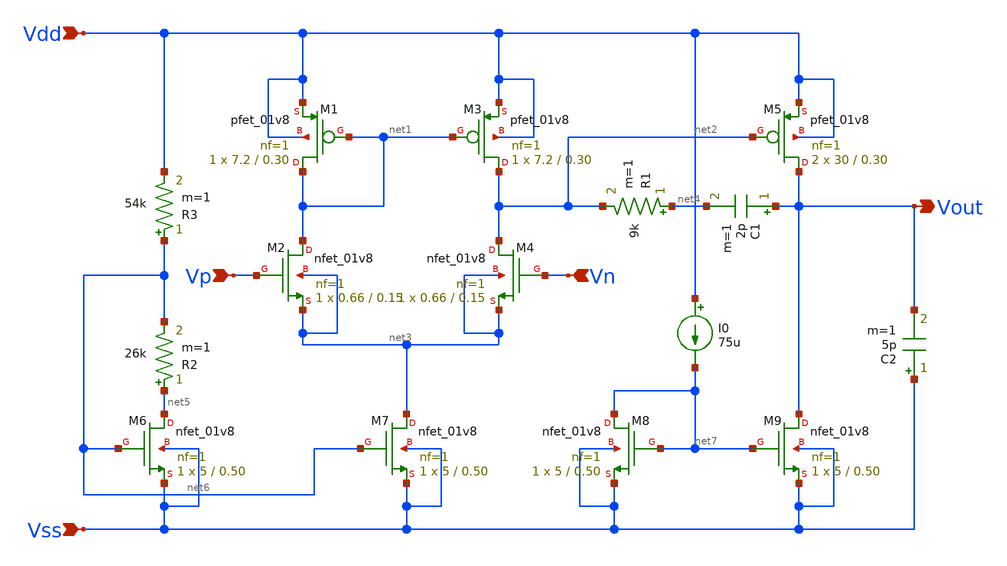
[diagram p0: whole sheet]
** sch_path: Bandgap/No_Ideal/two_stage.sch
**.subckt two_stage Vdd Vout Vss Vp Vn
*.ipin Vdd
*.opin Vout
*.ipin Vss
*.ipin Vp
*.ipin Vn
XM1 net1 net1 Vdd Vdd sky130_fd_pr__pfet_01v8 L=0.30 W=7.2 nf=1 ad='int((1 + 1)/2) * 7.2 / 1 * 0.29'
+ as='int((1 + 2)/2) * 7.2 / 1 * 0.29' pd='2*int((1 + 1)/2) * (7.2 / 1 + 0.29)' ps='2*int((1 + 2)/2) * (7.2 / 1 + 0.29)'
+ nrd='0.29 / 7.2 ' nrs='0.29 / 7.2 ' sa=0 sb=0 sd=0 mult=1 m=1
XM2 net1 Vp net3 net3 sky130_fd_pr__nfet_01v8 L=0.15 W=0.66 nf=1 ad='int((1 + 1)/2) * 0.66 / 1 * 0.29'
+ as='int((1 + 2)/2) * 0.66 / 1 * 0.29' pd='2*int((1 + 1)/2) * (0.66 / 1 + 0.29)' ps='2*int((1 + 2)/2) * (0.66 / 1 + 0.29)'
+ nrd='0.29 / 0.66 ' nrs='0.29 / 0.66 ' sa=0 sb=0 sd=0 mult=1 m=1
XM3 net2 net1 Vdd Vdd sky130_fd_pr__pfet_01v8 L=0.30 W=7.2 nf=1 ad='int((1 + 1)/2) * 7.2 / 1 * 0.29'
+ as='int((1 + 2)/2) * 7.2 / 1 * 0.29' pd='2*int((1 + 1)/2) * (7.2 / 1 + 0.29)' ps='2*int((1 + 2)/2) * (7.2 / 1 + 0.29)'
+ nrd='0.29 / 7.2 ' nrs='0.29 / 7.2 ' sa=0 sb=0 sd=0 mult=1 m=1
XM4 net2 Vn net3 net3 sky130_fd_pr__nfet_01v8 L=0.15 W=0.66 nf=1 ad='int((1 + 1)/2) * 0.66 / 1 * 0.29'
+ as='int((1 + 2)/2) * 0.66 / 1 * 0.29' pd='2*int((1 + 1)/2) * (0.66 / 1 + 0.29)' ps='2*int((1 + 2)/2) * (0.66 / 1 + 0.29)'
+ nrd='0.29 / 0.66 ' nrs='0.29 / 0.66 ' sa=0 sb=0 sd=0 mult=1 m=1
XM5 Vout net2 Vdd Vdd sky130_fd_pr__pfet_01v8 L=0.30 W=30 nf=1 ad='int((1 + 1)/2) * 30 / 1 * 0.29' as='int((1 + 2)/2) * 30 / 1 * 0.29'
+ pd='2*int((1 + 1)/2) * (30 / 1 + 0.29)' ps='2*int((1 + 2)/2) * (30 / 1 + 0.29)' nrd='0.29 / 30 ' nrs='0.29 / 30 '
+ sa=0 sb=0 sd=0 mult=2 m=2
C1 Vout net4 2p m=1
R1 net4 net2 9k m=1
C2 Vss Vout 5p m=1
R2 net5 net6 26k m=1
R3 net6 Vdd 54k m=1
XM6 net5 net6 Vss Vss sky130_fd_pr__nfet_01v8 L=0.50 W=5 nf=1 ad='int((1 + 1)/2) * 5 / 1 * 0.29' as='int((1 + 2)/2) * 5 / 1 * 0.29'
+ pd='2*int((1 + 1)/2) * (5 / 1 + 0.29)' ps='2*int((1 + 2)/2) * (5 / 1 + 0.29)' nrd='0.29 / 5 ' nrs='0.29 / 5 '
+ sa=0 sb=0 sd=0 mult=1 m=1
XM7 net3 net6 Vss Vss sky130_fd_pr__nfet_01v8 L=0.50 W=5 nf=1 ad='int((1 + 1)/2) * 5 / 1 * 0.29' as='int((1 + 2)/2) * 5 / 1 * 0.29'
+ pd='2*int((1 + 1)/2) * (5 / 1 + 0.29)' ps='2*int((1 + 2)/2) * (5 / 1 + 0.29)' nrd='0.29 / 5 ' nrs='0.29 / 5 '
+ sa=0 sb=0 sd=0 mult=1 m=1
XM8 net7 net7 Vss Vss sky130_fd_pr__nfet_01v8 L=0.50 W=5 nf=1 ad='int((1 + 1)/2) * 5 / 1 * 0.29' as='int((1 + 2)/2) * 5 / 1 * 0.29'
+ pd='2*int((1 + 1)/2) * (5 / 1 + 0.29)' ps='2*int((1 + 2)/2) * (5 / 1 + 0.29)' nrd='0.29 / 5 ' nrs='0.29 / 5 '
+ sa=0 sb=0 sd=0 mult=1 m=1
XM9 Vout net7 Vss Vss sky130_fd_pr__nfet_01v8 L=0.50 W=5 nf=1 ad='int((1 + 1)/2) * 5 / 1 * 0.29' as='int((1 + 2)/2) * 5 / 1 * 0.29'
+ pd='2*int((1 + 1)/2) * (5 / 1 + 0.29)' ps='2*int((1 + 2)/2) * (5 / 1 + 0.29)' nrd='0.29 / 5 ' nrs='0.29 / 5 '
+ sa=0 sb=0 sd=0 mult=1 m=1
I0 Vdd net7 75u
**.ends
.end
